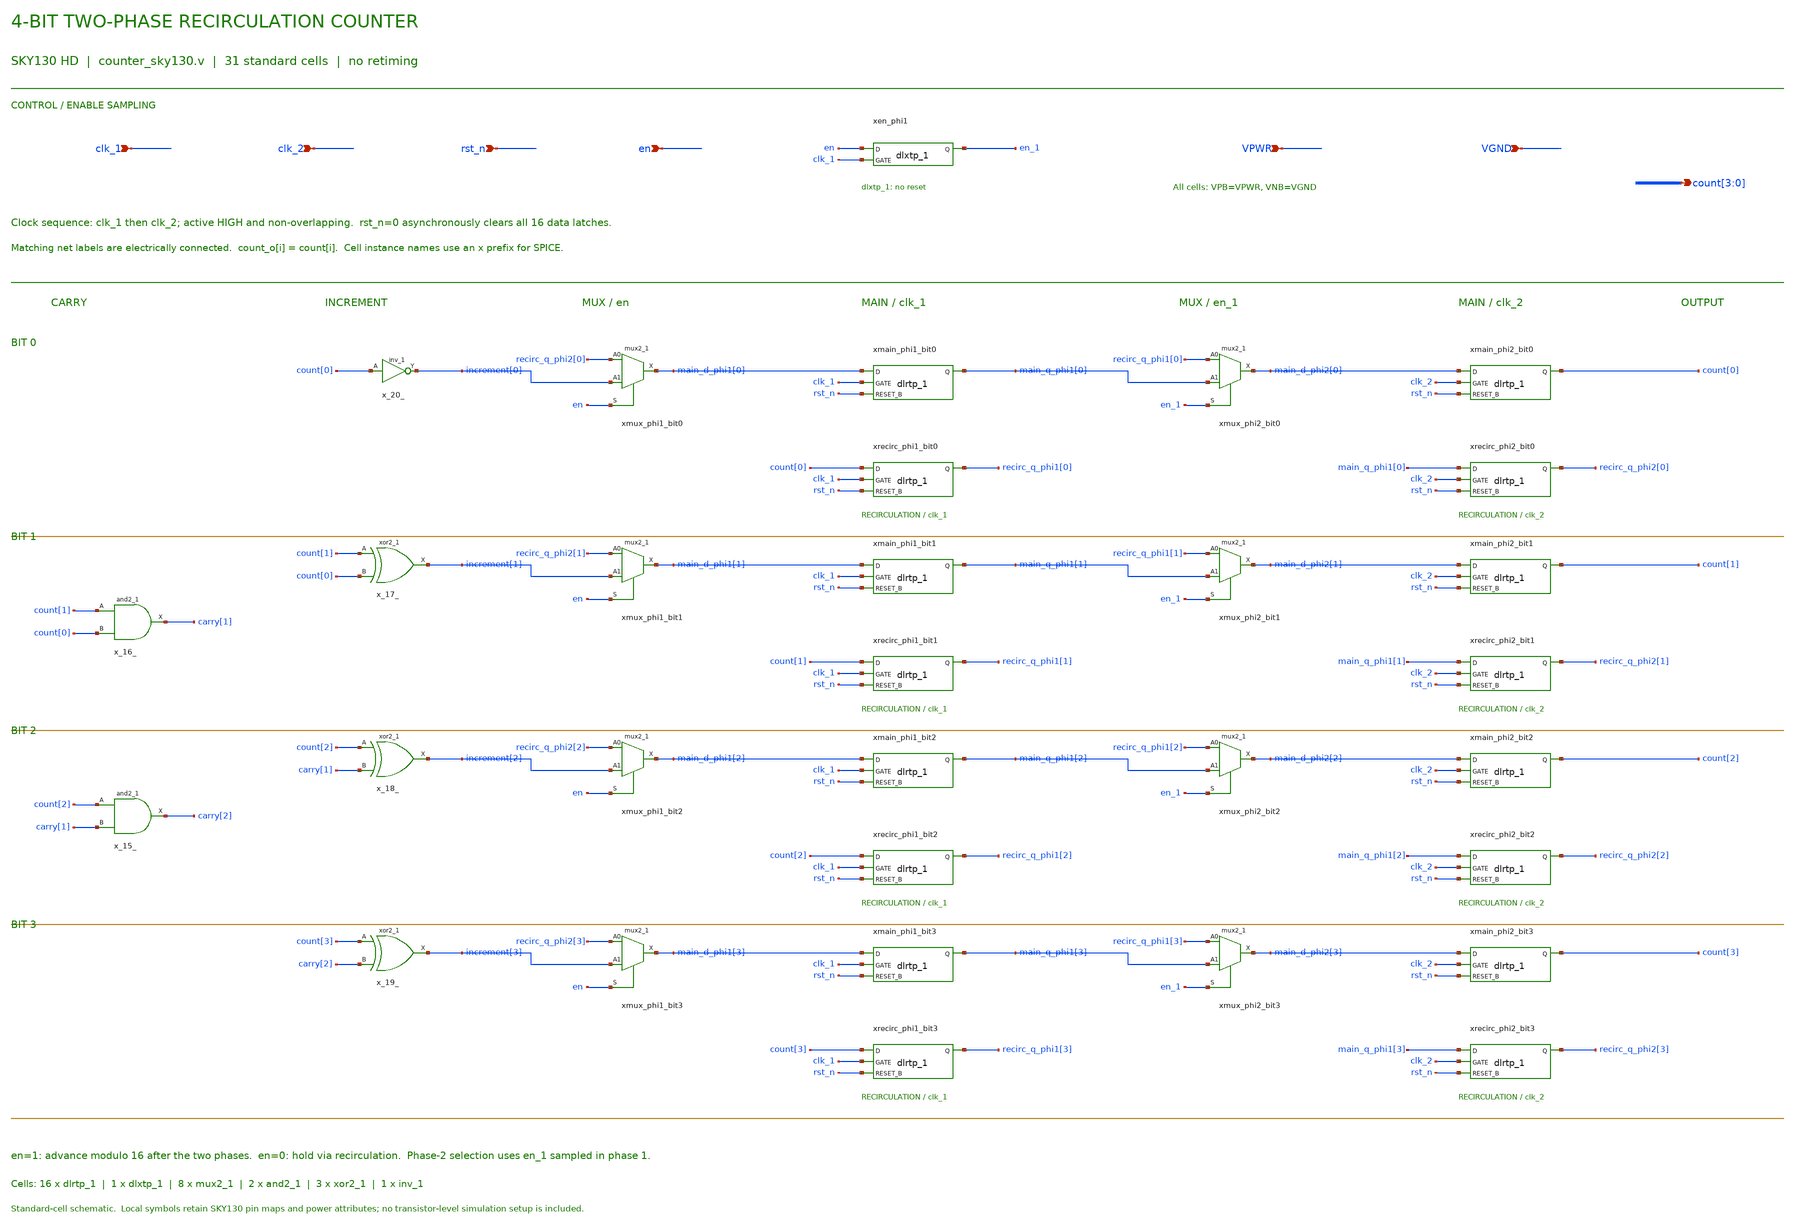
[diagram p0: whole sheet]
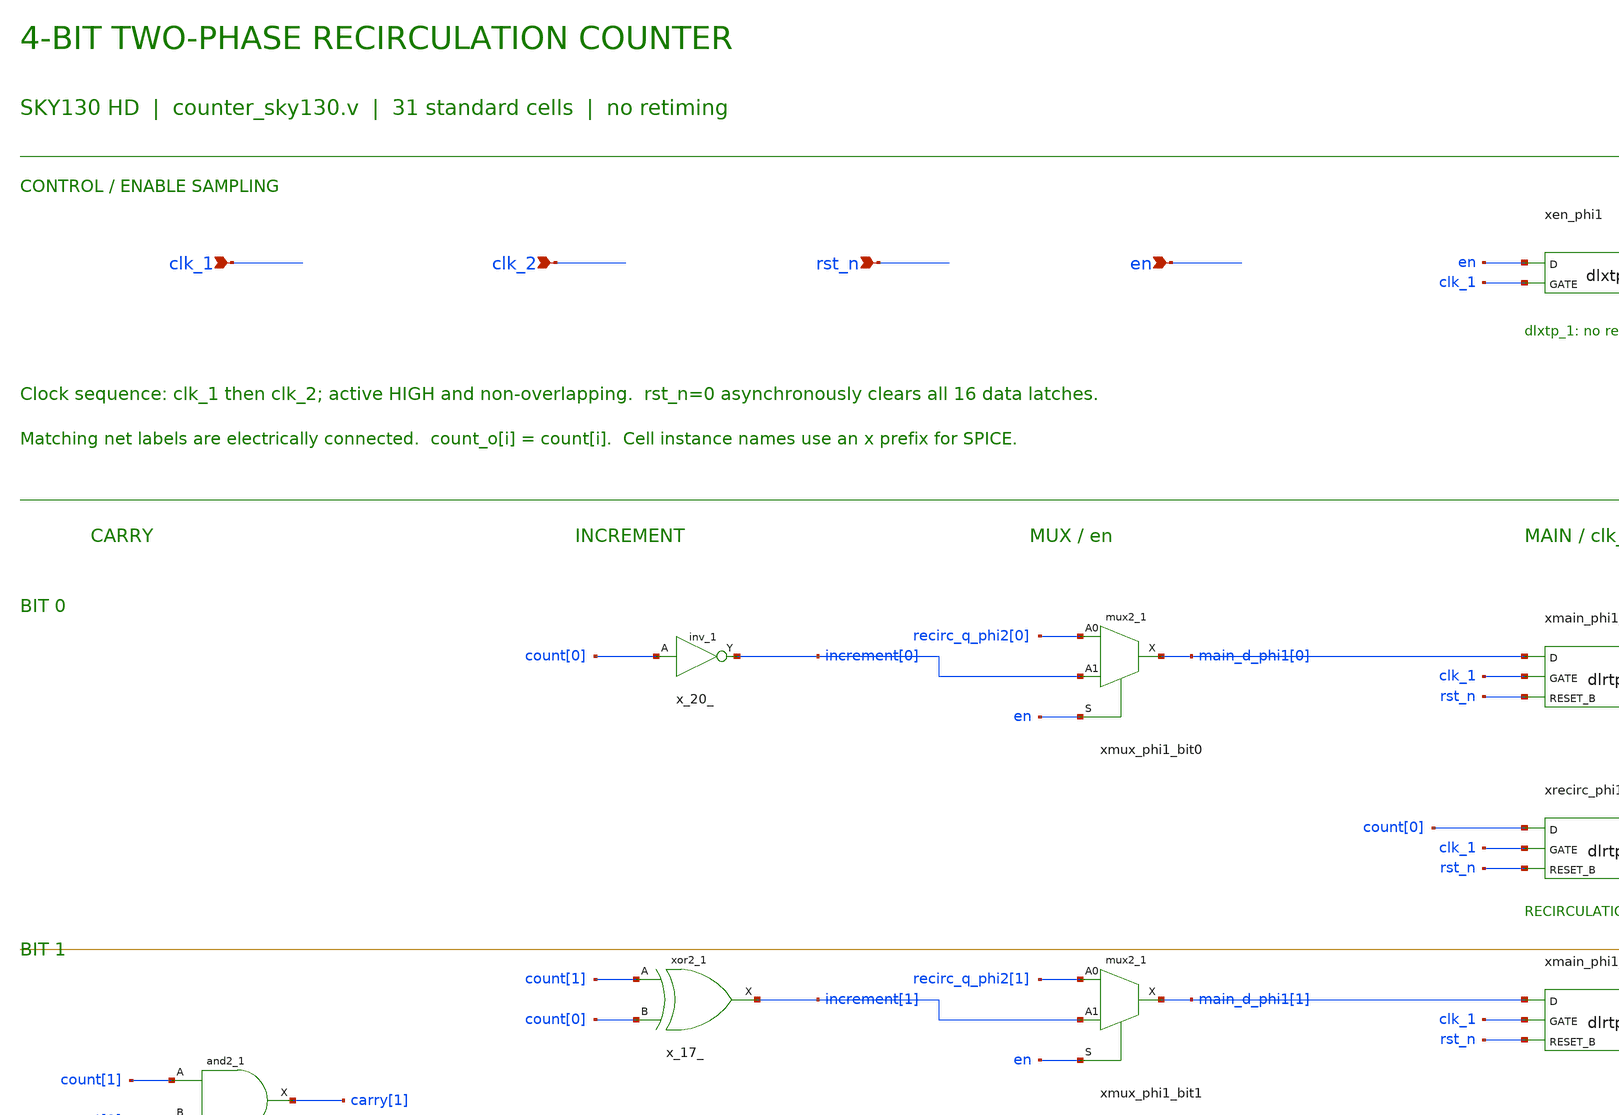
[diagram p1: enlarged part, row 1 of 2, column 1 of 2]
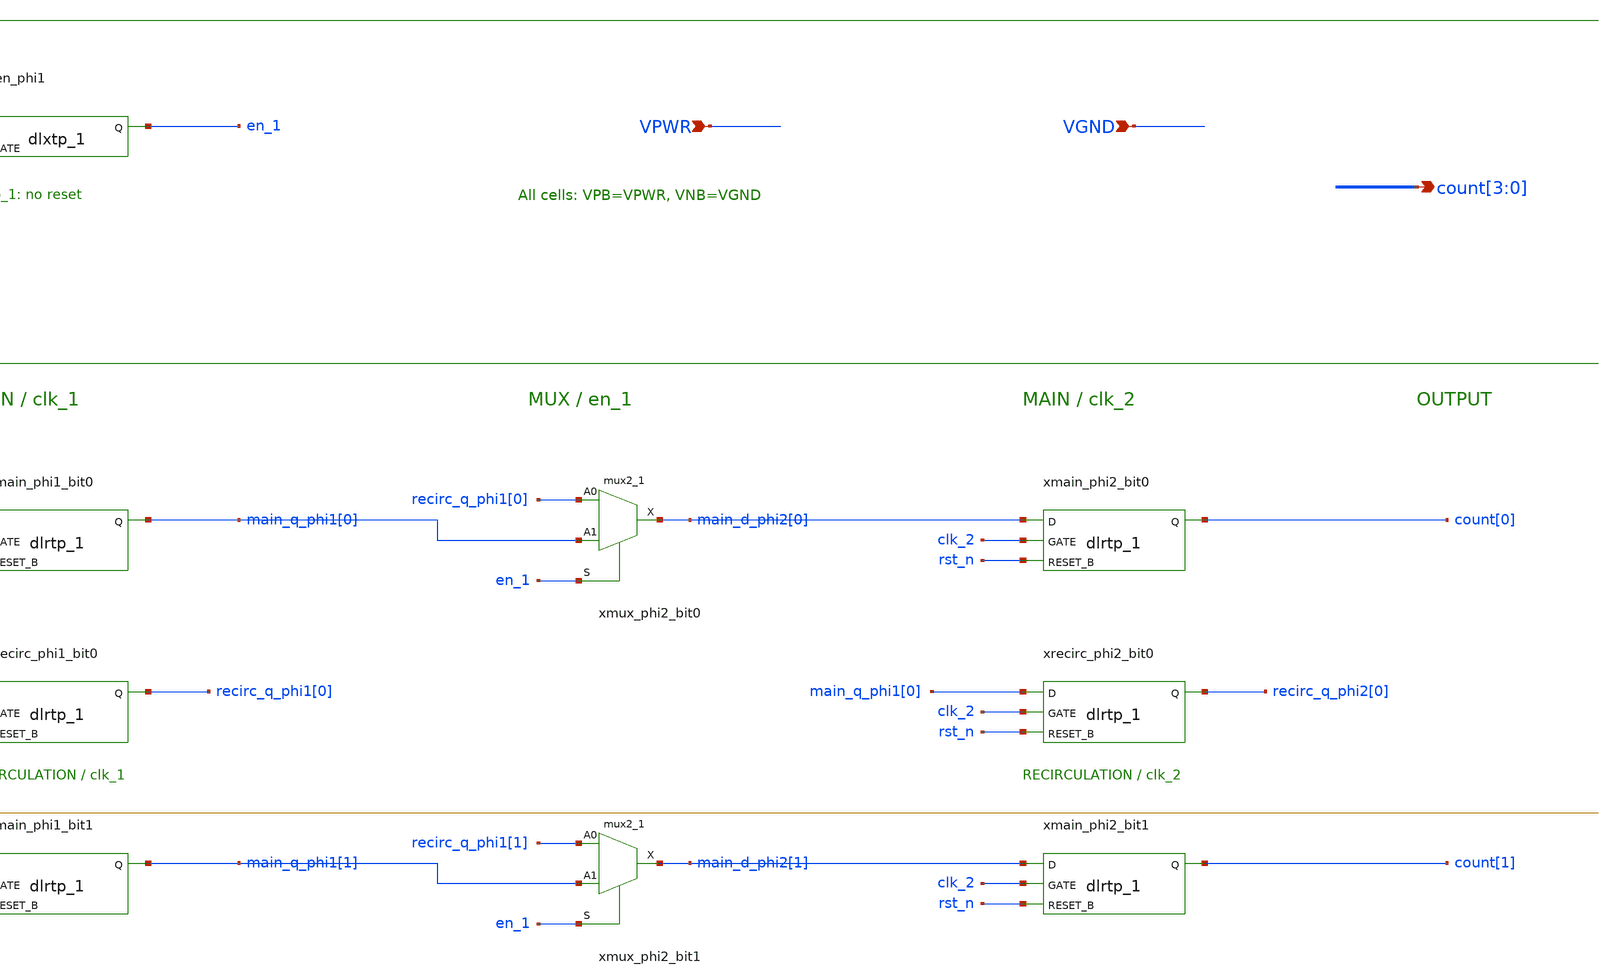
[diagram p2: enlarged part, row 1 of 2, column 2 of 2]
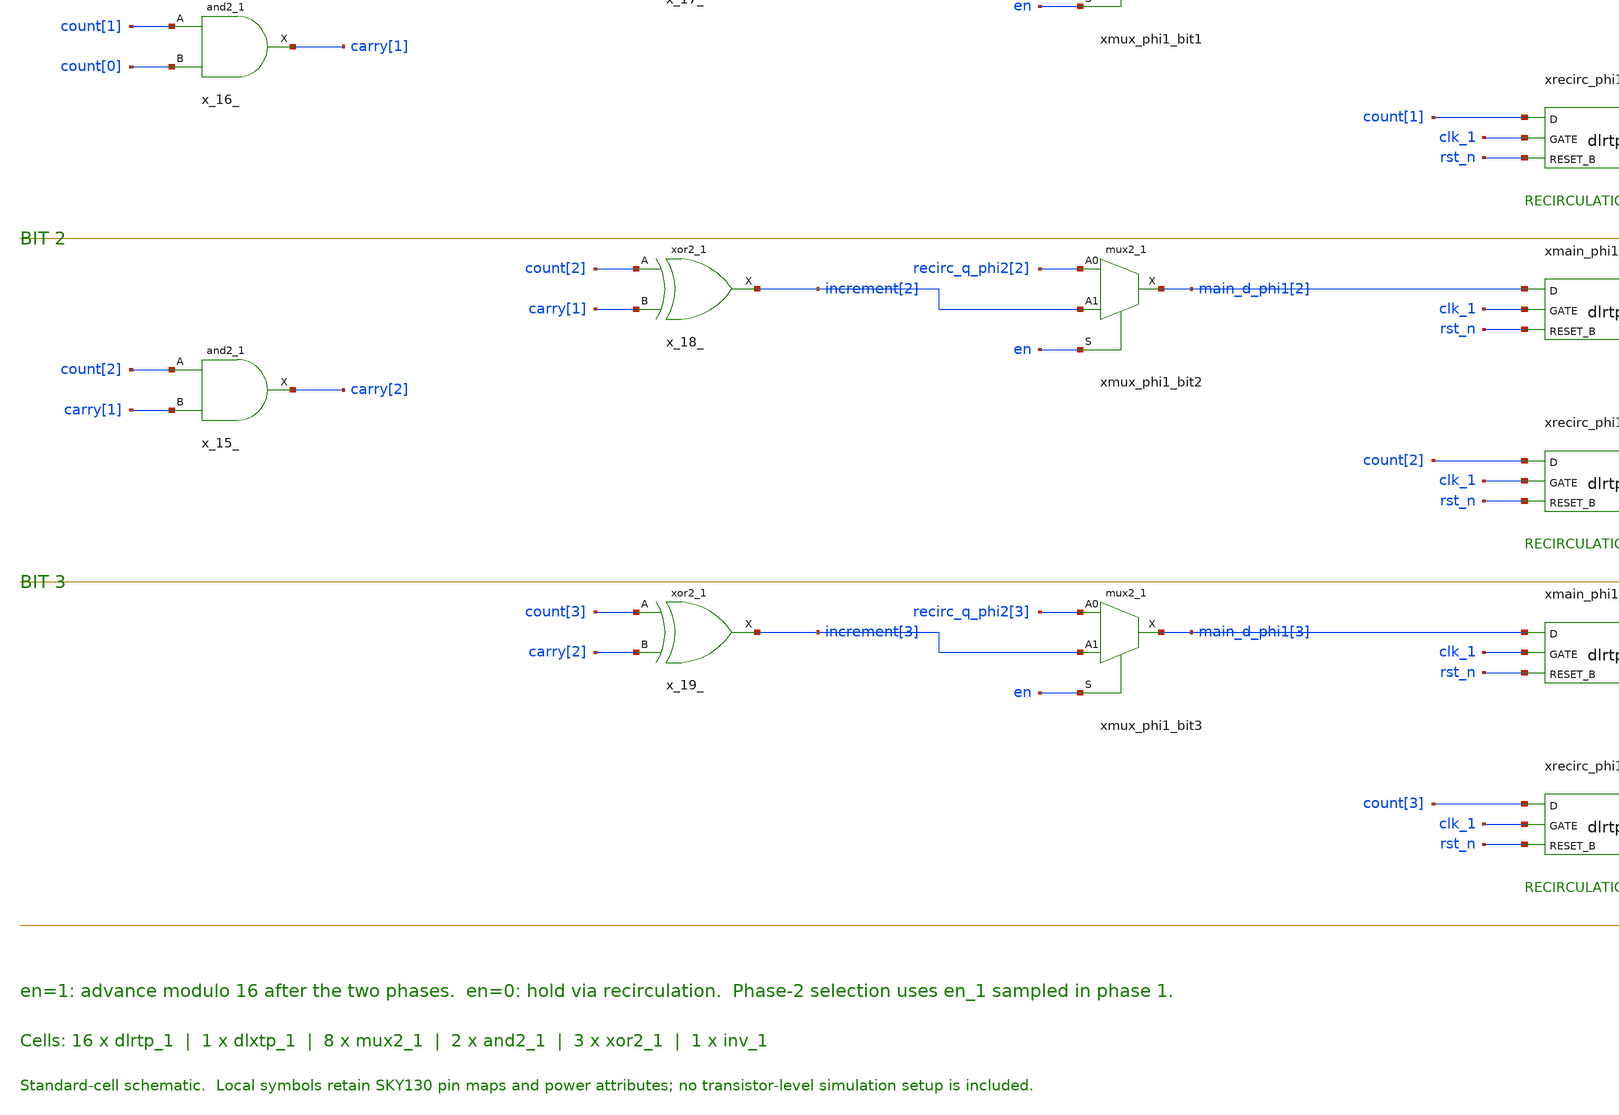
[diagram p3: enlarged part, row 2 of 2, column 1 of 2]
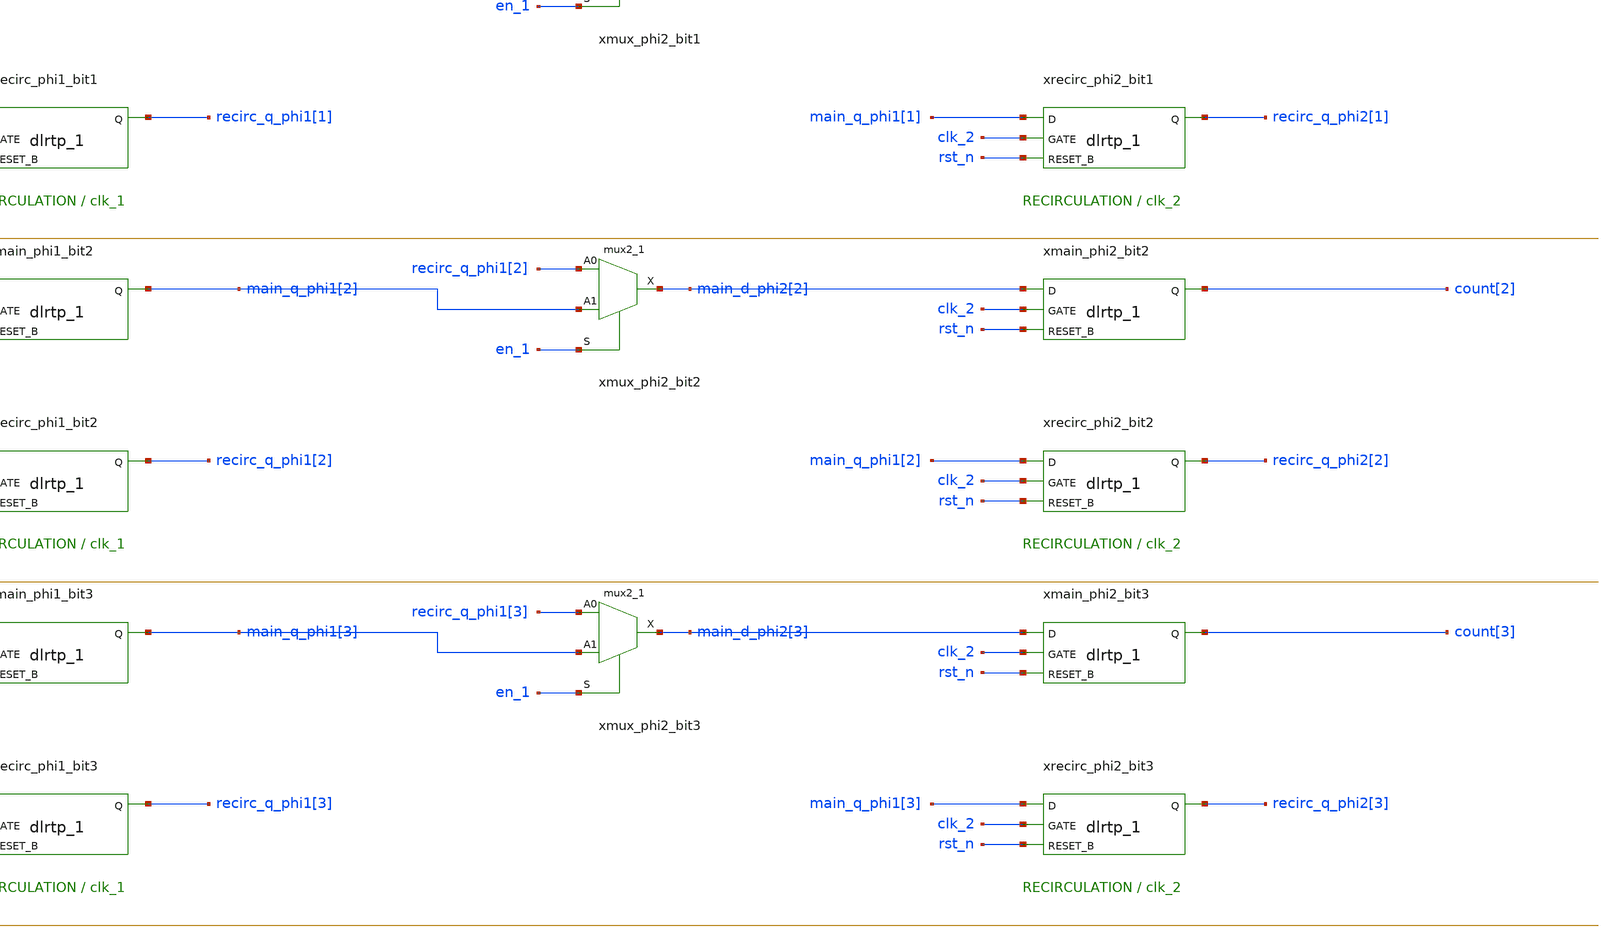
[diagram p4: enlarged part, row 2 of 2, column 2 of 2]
** sch_path: examples/counter/counter_latch_mux_2/counter_sky130.sch
**.subckt counter_sky130 clk_1 clk_2 rst_n en VPWR VGND count[3],count[2],count[1],count[0]
*.ipin clk_1
*.ipin clk_2
*.ipin rst_n
*.ipin en
*.ipin VPWR
*.ipin VGND
*.opin count[3],count[2],count[1],count[0]
xen_phi1 en clk_1 VGND VGND VPWR VPWR en_1 sky130_fd_sc_hd__dlxtp_1
x_20_ count[0] VGND VGND VPWR VPWR increment[0] sky130_fd_sc_hd__inv_1
xmux_phi1_bit0 recirc_q_phi2[0] increment[0] en VGND VGND VPWR VPWR main_d_phi1[0]
+ sky130_fd_sc_hd__mux2_1
xmain_phi1_bit0 main_d_phi1[0] clk_1 rst_n VGND VGND VPWR VPWR main_q_phi1[0]
+ sky130_fd_sc_hd__dlrtp_1
xmux_phi2_bit0 recirc_q_phi1[0] main_q_phi1[0] en_1 VGND VGND VPWR VPWR main_d_phi2[0]
+ sky130_fd_sc_hd__mux2_1
xmain_phi2_bit0 main_d_phi2[0] clk_2 rst_n VGND VGND VPWR VPWR count[0] sky130_fd_sc_hd__dlrtp_1
xrecirc_phi1_bit0 count[0] clk_1 rst_n VGND VGND VPWR VPWR recirc_q_phi1[0] sky130_fd_sc_hd__dlrtp_1
xrecirc_phi2_bit0 main_q_phi1[0] clk_2 rst_n VGND VGND VPWR VPWR recirc_q_phi2[0]
+ sky130_fd_sc_hd__dlrtp_1
x_17_ count[1] count[0] VGND VGND VPWR VPWR increment[1] sky130_fd_sc_hd__xor2_1
xmux_phi1_bit1 recirc_q_phi2[1] increment[1] en VGND VGND VPWR VPWR main_d_phi1[1]
+ sky130_fd_sc_hd__mux2_1
xmain_phi1_bit1 main_d_phi1[1] clk_1 rst_n VGND VGND VPWR VPWR main_q_phi1[1]
+ sky130_fd_sc_hd__dlrtp_1
xmux_phi2_bit1 recirc_q_phi1[1] main_q_phi1[1] en_1 VGND VGND VPWR VPWR main_d_phi2[1]
+ sky130_fd_sc_hd__mux2_1
xmain_phi2_bit1 main_d_phi2[1] clk_2 rst_n VGND VGND VPWR VPWR count[1] sky130_fd_sc_hd__dlrtp_1
xrecirc_phi1_bit1 count[1] clk_1 rst_n VGND VGND VPWR VPWR recirc_q_phi1[1] sky130_fd_sc_hd__dlrtp_1
xrecirc_phi2_bit1 main_q_phi1[1] clk_2 rst_n VGND VGND VPWR VPWR recirc_q_phi2[1]
+ sky130_fd_sc_hd__dlrtp_1
x_18_ count[2] carry[1] VGND VGND VPWR VPWR increment[2] sky130_fd_sc_hd__xor2_1
xmux_phi1_bit2 recirc_q_phi2[2] increment[2] en VGND VGND VPWR VPWR main_d_phi1[2]
+ sky130_fd_sc_hd__mux2_1
xmain_phi1_bit2 main_d_phi1[2] clk_1 rst_n VGND VGND VPWR VPWR main_q_phi1[2]
+ sky130_fd_sc_hd__dlrtp_1
xmux_phi2_bit2 recirc_q_phi1[2] main_q_phi1[2] en_1 VGND VGND VPWR VPWR main_d_phi2[2]
+ sky130_fd_sc_hd__mux2_1
xmain_phi2_bit2 main_d_phi2[2] clk_2 rst_n VGND VGND VPWR VPWR count[2] sky130_fd_sc_hd__dlrtp_1
xrecirc_phi1_bit2 count[2] clk_1 rst_n VGND VGND VPWR VPWR recirc_q_phi1[2] sky130_fd_sc_hd__dlrtp_1
xrecirc_phi2_bit2 main_q_phi1[2] clk_2 rst_n VGND VGND VPWR VPWR recirc_q_phi2[2]
+ sky130_fd_sc_hd__dlrtp_1
x_19_ count[3] carry[2] VGND VGND VPWR VPWR increment[3] sky130_fd_sc_hd__xor2_1
xmux_phi1_bit3 recirc_q_phi2[3] increment[3] en VGND VGND VPWR VPWR main_d_phi1[3]
+ sky130_fd_sc_hd__mux2_1
xmain_phi1_bit3 main_d_phi1[3] clk_1 rst_n VGND VGND VPWR VPWR main_q_phi1[3]
+ sky130_fd_sc_hd__dlrtp_1
xmux_phi2_bit3 recirc_q_phi1[3] main_q_phi1[3] en_1 VGND VGND VPWR VPWR main_d_phi2[3]
+ sky130_fd_sc_hd__mux2_1
xmain_phi2_bit3 main_d_phi2[3] clk_2 rst_n VGND VGND VPWR VPWR count[3] sky130_fd_sc_hd__dlrtp_1
xrecirc_phi1_bit3 count[3] clk_1 rst_n VGND VGND VPWR VPWR recirc_q_phi1[3] sky130_fd_sc_hd__dlrtp_1
xrecirc_phi2_bit3 main_q_phi1[3] clk_2 rst_n VGND VGND VPWR VPWR recirc_q_phi2[3]
+ sky130_fd_sc_hd__dlrtp_1
x_16_ count[1] count[0] VGND VGND VPWR VPWR carry[1] sky130_fd_sc_hd__and2_1
x_15_ count[2] carry[1] VGND VGND VPWR VPWR carry[2] sky130_fd_sc_hd__and2_1
**.ends
.end
